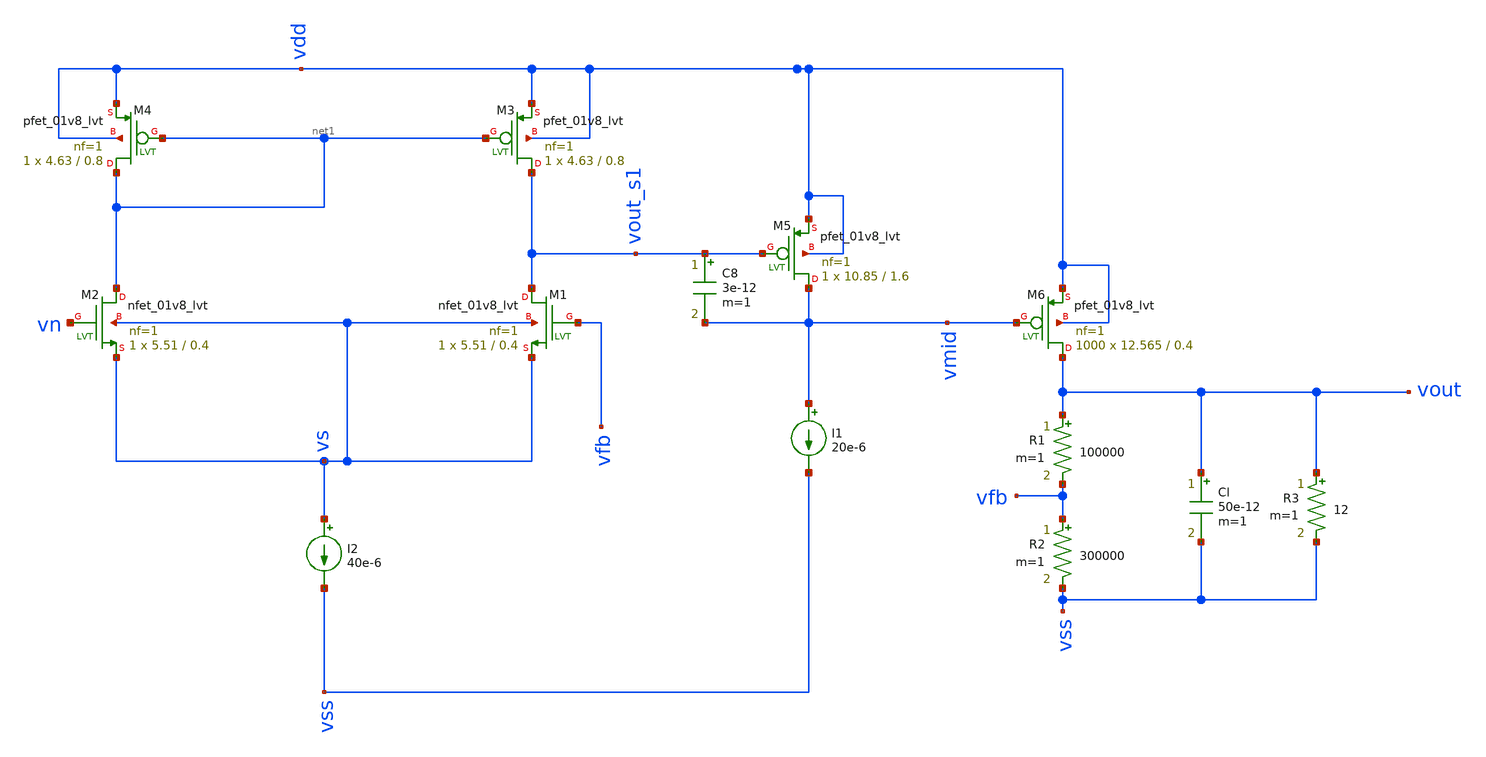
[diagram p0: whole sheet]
** sch_path: test-python/sstadex/xschem/ldo_final_tb.sch
**.subckt ldo_final_tb
I2 vs vss 40e-6
XM1 vout_s1 vfb vs vs sky130_fd_pr__nfet_01v8_lvt L=0.4 W=5.51 nf=1 ad='int((nf+1)/2) * W/nf * 0.29'
+ as='int((nf+2)/2) * W/nf * 0.29' pd='2*int((nf+1)/2) * (W/nf + 0.29)' ps='2*int((nf+2)/2) * (W/nf + 0.29)'
+ nrd='0.29 / W' nrs='0.29 / W' sa=0 sb=0 sd=0 mult=1 m=1
XM2 net1 vn vs vs sky130_fd_pr__nfet_01v8_lvt L=0.4 W=5.51 nf=1 ad='int((nf+1)/2) * W/nf * 0.29' as='int((nf+2)/2) * W/nf * 0.29'
+ pd='2*int((nf+1)/2) * (W/nf + 0.29)' ps='2*int((nf+2)/2) * (W/nf + 0.29)' nrd='0.29 / W' nrs='0.29 / W'
+ sa=0 sb=0 sd=0 mult=1 m=1
XM3 vout_s1 net1 vdd vdd sky130_fd_pr__pfet_01v8_lvt L=0.8 W=4.63 nf=1 ad='int((nf+1)/2) * W/nf * 0.29'
+ as='int((nf+2)/2) * W/nf * 0.29' pd='2*int((nf+1)/2) * (W/nf + 0.29)' ps='2*int((nf+2)/2) * (W/nf + 0.29)'
+ nrd='0.29 / W' nrs='0.29 / W' sa=0 sb=0 sd=0 mult=1 m=1
XM4 net1 net1 vdd vdd sky130_fd_pr__pfet_01v8_lvt L=0.8 W=4.63 nf=1 ad='int((nf+1)/2) * W/nf * 0.29'
+ as='int((nf+2)/2) * W/nf * 0.29' pd='2*int((nf+1)/2) * (W/nf + 0.29)' ps='2*int((nf+2)/2) * (W/nf + 0.29)'
+ nrd='0.29 / W' nrs='0.29 / W' sa=0 sb=0 sd=0 mult=1 m=1
XM5 vmid vout_s1 vdd vdd sky130_fd_pr__pfet_01v8_lvt L=1.6 W=10.85 nf=1 ad='int((nf+1)/2) * W/nf * 0.29'
+ as='int((nf+2)/2) * W/nf * 0.29' pd='2*int((nf+1)/2) * (W/nf + 0.29)' ps='2*int((nf+2)/2) * (W/nf + 0.29)'
+ nrd='0.29 / W' nrs='0.29 / W' sa=0 sb=0 sd=0 mult=1 m=1
I1 vmid vss 20e-6
C8 vout_s1 vmid 3e-12 m=1
XM6 vout vmid vdd vdd sky130_fd_pr__pfet_01v8_lvt L=0.4 W=12.565 nf=1 ad='int((nf+1)/2) * W/nf * 0.29'
+ as='int((nf+2)/2) * W/nf * 0.29' pd='2*int((nf+1)/2) * (W/nf + 0.29)' ps='2*int((nf+2)/2) * (W/nf + 0.29)'
+ nrd='0.29 / W' nrs='0.29 / W' sa=0 sb=0 sd=0 mult=1000 m=1000
R1 vout vfb 100000 m=1
R2 vfb vss 300000 m=1
Cl vout vss 50e-12 m=1
R3 vout vss 12 m=1
**** begin user architecture code



.lib /opt/pdks/sky130A/libs.tech/ngspice/sky130.lib.spice tt

Vref vn 0 dc 0.9
Vdd vdd 0 1.8 ac 1
Vss vss 0 0

.control
ac dec 10 1 100G
plot vdb(vout)
plot phase(vout)
op
print vout vmid vout_s1 vs
print @m.xm6.msky130_fd_pr__pfet_01v8_lvt[id]
.endc

.control
tran 10n 1u
plot vout vs vmid Vmeas
.endc



**** end user architecture code
**.ends
.end
